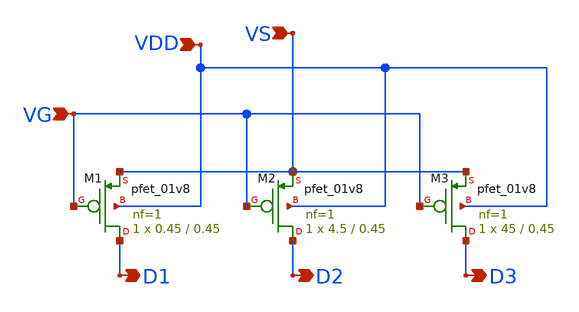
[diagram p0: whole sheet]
** sch_path: sky130_cells/FETs/alexpmos/one_to_hundred.sch
**.subckt one_to_hundred VS D1 D2 D3 VDD VG
*.ipin VS
*.opin D1
*.opin D2
*.opin D3
*.ipin VDD
*.ipin VG
XM1 D1 VG VS VDD sky130_fd_pr__pfet_01v8 L=0.45 W=0.45 nf=1 ad='int((nf+1)/2) * W/nf * 0.29' as='int((nf+2)/2) * W/nf * 0.29'
+ pd='2*int((nf+1)/2) * (W/nf + 0.29)' ps='2*int((nf+2)/2) * (W/nf + 0.29)' nrd='0.29 / W' nrs='0.29 / W'
+ sa=0 sb=0 sd=0 mult=1 m=1
XM2 D2 VG VS VDD sky130_fd_pr__pfet_01v8 L=0.45 W=4.5 nf=1 ad='int((nf+1)/2) * W/nf * 0.29' as='int((nf+2)/2) * W/nf * 0.29'
+ pd='2*int((nf+1)/2) * (W/nf + 0.29)' ps='2*int((nf+2)/2) * (W/nf + 0.29)' nrd='0.29 / W' nrs='0.29 / W'
+ sa=0 sb=0 sd=0 mult=1 m=1
XM3 D3 VG VS VDD sky130_fd_pr__pfet_01v8 L=0.45 W=45 nf=1 ad='int((nf+1)/2) * W/nf * 0.29' as='int((nf+2)/2) * W/nf * 0.29'
+ pd='2*int((nf+1)/2) * (W/nf + 0.29)' ps='2*int((nf+2)/2) * (W/nf + 0.29)' nrd='0.29 / W' nrs='0.29 / W'
+ sa=0 sb=0 sd=0 mult=1 m=1
**.ends
.end
